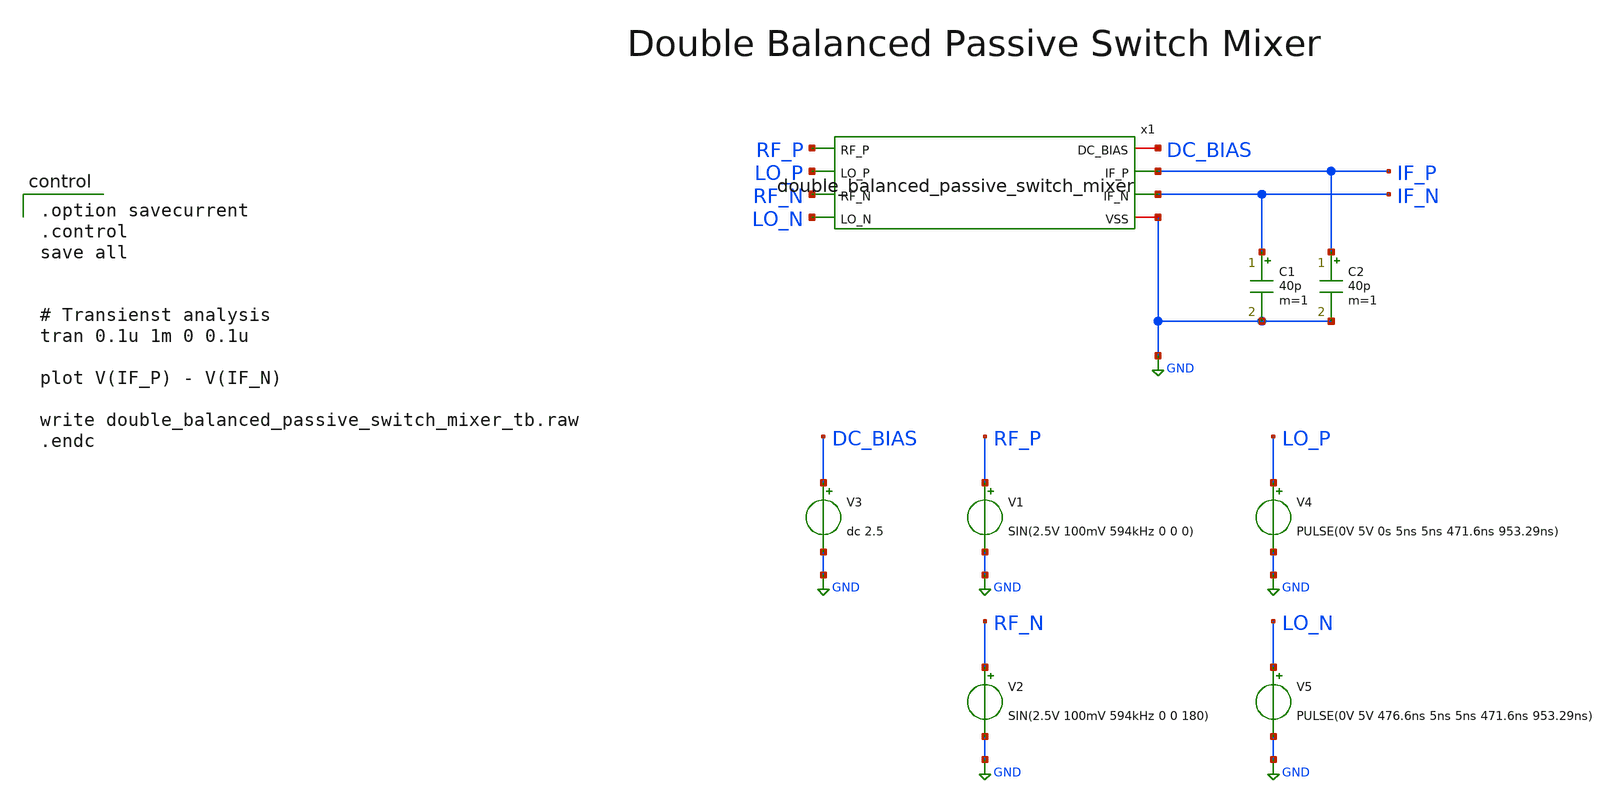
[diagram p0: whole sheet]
** sch_path: member_project/MIXER/noritsuna/xschem/double_balanced_passive_switch_mixer_tb.sch
**.subckt double_balanced_passive_switch_mixer_tb
V3 DC_BIAS GND dc 2.5
C1 IF_N GND 40p m=1
C2 IF_P GND 40p m=1
V1 RF_P GND SIN(2.5V 100mV 594kHz 0 0 0)
V2 RF_N GND SIN(2.5V 100mV 594kHz 0 0 180)
V4 LO_P GND PULSE(0V 5V 0s 5ns 5ns 471.6ns 953.29ns)
V5 LO_N GND PULSE(0V 5V 476.6ns 5ns 5ns 471.6ns 953.29ns)
x1 DC_BIAS RF_P LO_P RF_N LO_N IF_P IF_N GND double_balanced_passive_switch_mixer
**** begin user architecture code
 .include $::LIB/ip62_models

.option savecurrent
.control
save all


# Transienst analysis
tran 0.1u 1m 0 0.1u

plot V(IF_P) - V(IF_N)

write double_balanced_passive_switch_mixer_tb.raw
.endc

**** end user architecture code
**.ends

* expanding   symbol:  double_balanced_passive_switch_mixer.sym # of pins=8
** sym_path: member_project/MIXER/noritsuna/xschem/double_balanced_passive_switch_mixer.sym
** sch_path: member_project/MIXER/noritsuna/xschem/double_balanced_passive_switch_mixer.sch
.subckt double_balanced_passive_switch_mixer DC_BIAS RF_P LO_P RF_N LO_N IF_P IF_N VSS
*.iopin DC_BIAS
*.ipin RF_P
*.ipin LO_P
*.ipin RF_N
*.ipin LO_N
*.opin IF_N
*.opin IF_P
*.iopin VSS
XXM1 RF_P LO_P IF_P VSS NMOS w=100u l=1u nrd=0 nrs=0 m=1
XXM2 RF_P LO_N IF_N VSS NMOS w=100u l=1u nrd=0 nrs=0 m=1
XXM3 RF_N LO_N IF_P VSS NMOS w=100u l=1u nrd=0 nrs=0 m=1
XXM4 RF_N LO_P IF_N VSS NMOS w=100u l=1u nrd=0 nrs=0 m=1
XR1 DC_BIAS RF_P DC_BIAS F_RR w=2.8e-06 l=49.4e-06 R=20.0e+03 tc1=0 tc2=0 m=1
XR2 DC_BIAS IF_P DC_BIAS F_RR w=2.8e-06 l=49.4e-06 R=20.0e+03 tc1=0 tc2=0 m=1
XXC1 IF_P VSS VSS F_CSIO c=4.86p x=90u y=90u m=4
XXC2 IF_N VSS VSS F_CSIO c=4.86p x=90u y=90u m=4
XR3 DC_BIAS IF_N DC_BIAS F_RR w=2.8e-06 l=49.4e-06 R=20.0e+03 tc1=0 tc2=0 m=1
XXM6 IF_P VSS VSS VSS NMOS w=10u l=1u nrd=0 nrs=0 m=4
XXM7 IF_N VSS VSS VSS NMOS w=10u l=1u nrd=0 nrs=0 m=4
.ends

.GLOBAL GND
.end
